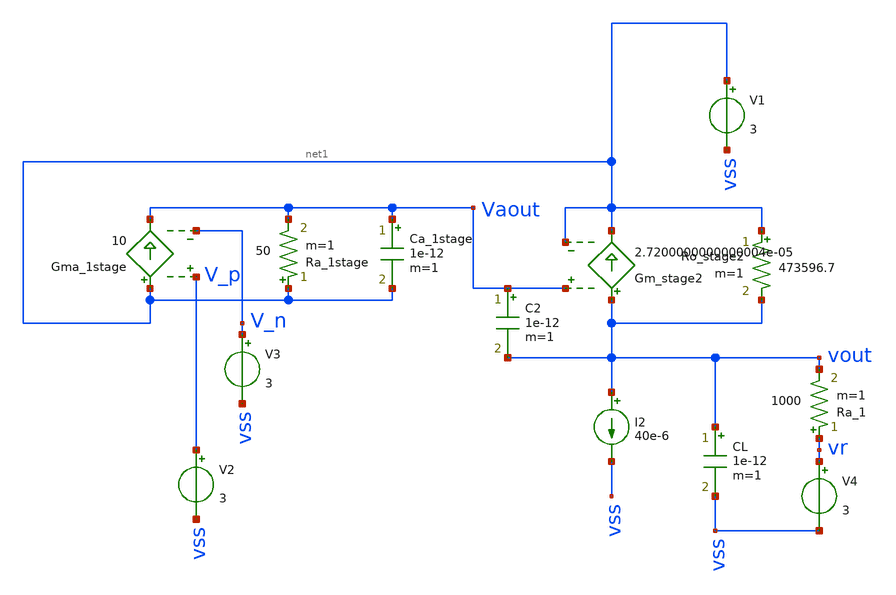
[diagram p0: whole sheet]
** sch_path: test-python/sstadex/xschem/stage2_OTA_r.sch
**.subckt stage2_OTA_r
Ro_stage2 net1 vout 473596.7 m=1
Gm_stage2 vout net1 Vaout net1 2.7200000000000004e-05
Gma_1stage net1 Vaout V_p V_n 10
Ra_1stage net1 Vaout 50 m=1
V1 net1 vss 3
V3 V_n vss 3
I2 vout vss 40e-6
V2 V_p vss 3
CL vout vss 1e-12 m=1
C2 Vaout vout 1e-12 m=1
Ca_1stage Vaout net1 1e-12 m=1
V4 vr vss 3
Ra_1 vr vout 1000 m=1
**.ends
.end
